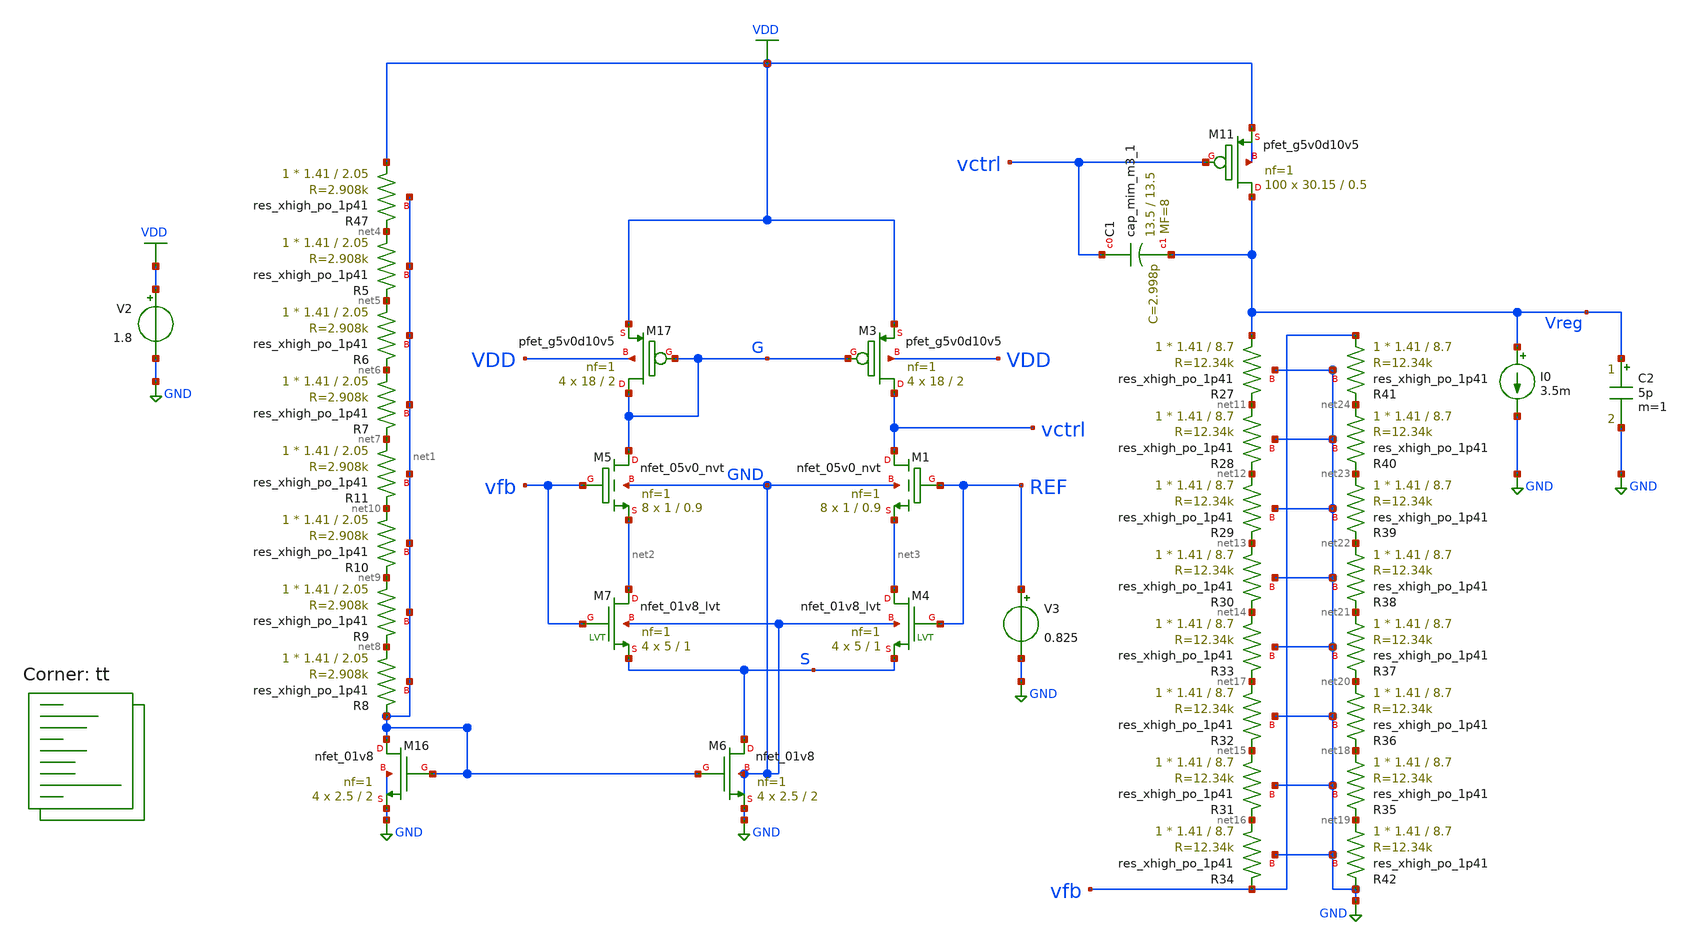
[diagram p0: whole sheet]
** sch_path: ALDO/Schematic/Testbenches/LDO4_stef.sch
**.subckt LDO4_stef
XM11 Vreg vctrl VDD VDD sky130_fd_pr__pfet_g5v0d10v5 L=0.5 W=30.15 nf=1 ad='int((nf+1)/2) * W/nf * 0.29'
+ as='int((nf+2)/2) * W/nf * 0.29' pd='2*int((nf+1)/2) * (W/nf + 0.29)' ps='2*int((nf+2)/2) * (W/nf + 0.29)'
+ nrd='0.29 / W' nrs='0.29 / W' sa=0 sb=0 sd=0 mult=100 m=100
V3 REF GND 0.825
C2 Vreg GND 5p m=1
XM16 net1 net1 GND GND sky130_fd_pr__nfet_01v8 L=2 W=2.5 nf=1 ad='int((nf+1)/2) * W/nf * 0.29' as='int((nf+2)/2) * W/nf * 0.29'
+ pd='2*int((nf+1)/2) * (W/nf + 0.29)' ps='2*int((nf+2)/2) * (W/nf + 0.29)' nrd='0.29 / W' nrs='0.29 / W'
+ sa=0 sb=0 sd=0 mult=4 m=4
XM3 vctrl G VDD VDD sky130_fd_pr__pfet_g5v0d10v5 L=2 W=18 nf=1 ad='int((nf+1)/2) * W/nf * 0.29' as='int((nf+2)/2) * W/nf * 0.29'
+ pd='2*int((nf+1)/2) * (W/nf + 0.29)' ps='2*int((nf+2)/2) * (W/nf + 0.29)' nrd='0.29 / W' nrs='0.29 / W'
+ sa=0 sb=0 sd=0 mult=4 m=4
XM17 G G VDD VDD sky130_fd_pr__pfet_g5v0d10v5 L=2 W=18 nf=1 ad='int((nf+1)/2) * W/nf * 0.29' as='int((nf+2)/2) * W/nf * 0.29'
+ pd='2*int((nf+1)/2) * (W/nf + 0.29)' ps='2*int((nf+2)/2) * (W/nf + 0.29)' nrd='0.29 / W' nrs='0.29 / W'
+ sa=0 sb=0 sd=0 mult=4 m=4
XR47 VDD net4 net1 sky130_fd_pr__res_xhigh_po_1p41 L=2.05 mult=1 m=1
XR5 net4 net5 net1 sky130_fd_pr__res_xhigh_po_1p41 L=2.05 mult=1 m=1
XR6 net5 net6 net1 sky130_fd_pr__res_xhigh_po_1p41 L=2.05 mult=1 m=1
XR7 net6 net7 net1 sky130_fd_pr__res_xhigh_po_1p41 L=2.05 mult=1 m=1
XR8 net8 net1 net1 sky130_fd_pr__res_xhigh_po_1p41 L=2.05 mult=1 m=1
XR9 net9 net8 net1 sky130_fd_pr__res_xhigh_po_1p41 L=2.05 mult=1 m=1
XR10 net10 net9 net1 sky130_fd_pr__res_xhigh_po_1p41 L=2.05 mult=1 m=1
XR11 net7 net10 net1 sky130_fd_pr__res_xhigh_po_1p41 L=2.05 mult=1 m=1
XR27 Vreg net11 GND sky130_fd_pr__res_xhigh_po_1p41 L=8.7 mult=1 m=1
XR28 net11 net12 GND sky130_fd_pr__res_xhigh_po_1p41 L=8.7 mult=1 m=1
XR29 net12 net13 GND sky130_fd_pr__res_xhigh_po_1p41 L=8.7 mult=1 m=1
XR30 net13 net14 GND sky130_fd_pr__res_xhigh_po_1p41 L=8.7 mult=1 m=1
XR31 net15 net16 GND sky130_fd_pr__res_xhigh_po_1p41 L=8.7 mult=1 m=1
XR32 net17 net15 GND sky130_fd_pr__res_xhigh_po_1p41 L=8.7 mult=1 m=1
XR33 net14 net17 GND sky130_fd_pr__res_xhigh_po_1p41 L=8.7 mult=1 m=1
XR34 net16 vfb GND sky130_fd_pr__res_xhigh_po_1p41 L=8.7 mult=1 m=1
XR35 net18 net19 GND sky130_fd_pr__res_xhigh_po_1p41 L=8.7 mult=1 m=1
XR36 net20 net18 GND sky130_fd_pr__res_xhigh_po_1p41 L=8.7 mult=1 m=1
XR37 net21 net20 GND sky130_fd_pr__res_xhigh_po_1p41 L=8.7 mult=1 m=1
XR38 net22 net21 GND sky130_fd_pr__res_xhigh_po_1p41 L=8.7 mult=1 m=1
XR39 net23 net22 GND sky130_fd_pr__res_xhigh_po_1p41 L=8.7 mult=1 m=1
XR40 net24 net23 GND sky130_fd_pr__res_xhigh_po_1p41 L=8.7 mult=1 m=1
XR41 vfb net24 GND sky130_fd_pr__res_xhigh_po_1p41 L=8.7 mult=1 m=1
XR42 net19 GND GND sky130_fd_pr__res_xhigh_po_1p41 L=8.7 mult=1 m=1
XC1 vctrl Vreg sky130_fd_pr__cap_mim_m3_1 W=13.5 L=13.5 MF=8 m=8
XM6 S net1 GND GND sky130_fd_pr__nfet_01v8 L=2 W=2.5 nf=1 ad='int((nf+1)/2) * W/nf * 0.29' as='int((nf+2)/2) * W/nf * 0.29'
+ pd='2*int((nf+1)/2) * (W/nf + 0.29)' ps='2*int((nf+2)/2) * (W/nf + 0.29)' nrd='0.29 / W' nrs='0.29 / W'
+ sa=0 sb=0 sd=0 mult=4 m=4
XM7 net2 vfb S GND sky130_fd_pr__nfet_01v8_lvt L=1 W=5 nf=1 ad='int((nf+1)/2) * W/nf * 0.29' as='int((nf+2)/2) * W/nf * 0.29'
+ pd='2*int((nf+1)/2) * (W/nf + 0.29)' ps='2*int((nf+2)/2) * (W/nf + 0.29)' nrd='0.29 / W' nrs='0.29 / W'
+ sa=0 sb=0 sd=0 mult=4 m=4
XM4 net3 REF S GND sky130_fd_pr__nfet_01v8_lvt L=1 W=5 nf=1 ad='int((nf+1)/2) * W/nf * 0.29' as='int((nf+2)/2) * W/nf * 0.29'
+ pd='2*int((nf+1)/2) * (W/nf + 0.29)' ps='2*int((nf+2)/2) * (W/nf + 0.29)' nrd='0.29 / W' nrs='0.29 / W'
+ sa=0 sb=0 sd=0 mult=4 m=4
V2 VDD GND 1.8
I0 Vreg GND 3.5m
XM5 G vfb net2 GND sky130_fd_pr__nfet_05v0_nvt L=0.9 W=1 nf=1 ad='int((nf+1)/2) * W/nf * 0.29' as='int((nf+2)/2) * W/nf * 0.29'
+ pd='2*int((nf+1)/2) * (W/nf + 0.29)' ps='2*int((nf+2)/2) * (W/nf + 0.29)' nrd='0.29 / W' nrs='0.29 / W'
+ sa=0 sb=0 sd=0 mult=8 m=8
XM1 vctrl REF net3 GND sky130_fd_pr__nfet_05v0_nvt L=0.9 W=1 nf=1 ad='int((nf+1)/2) * W/nf * 0.29' as='int((nf+2)/2) * W/nf * 0.29'
+ pd='2*int((nf+1)/2) * (W/nf + 0.29)' ps='2*int((nf+2)/2) * (W/nf + 0.29)' nrd='0.29 / W' nrs='0.29 / W'
+ sa=0 sb=0 sd=0 mult=8 m=8
**** begin user architecture code


.option wnflag=1
.option savecurrents sparse $ ITL1=2000 ITL2=500 GMINSTEPS=100
.temp 27
.control
save all
op
write LDO4_stef.raw
set appendwrite
**dc V1 0 3.3 10m
**dc I0 0.1m 3.5m 0.1m
**plot v(vreg)
write LDO4_stef.raw
tran 10n 10u 10n uic
write LDO4_stef.raw
plot v(vreg)
**quit 0
.endc


.lib $::SKYWATER_MODELS/sky130.lib.spice tt
**** end user architecture code
**.ends
.GLOBAL VDD
.GLOBAL GND
.end
